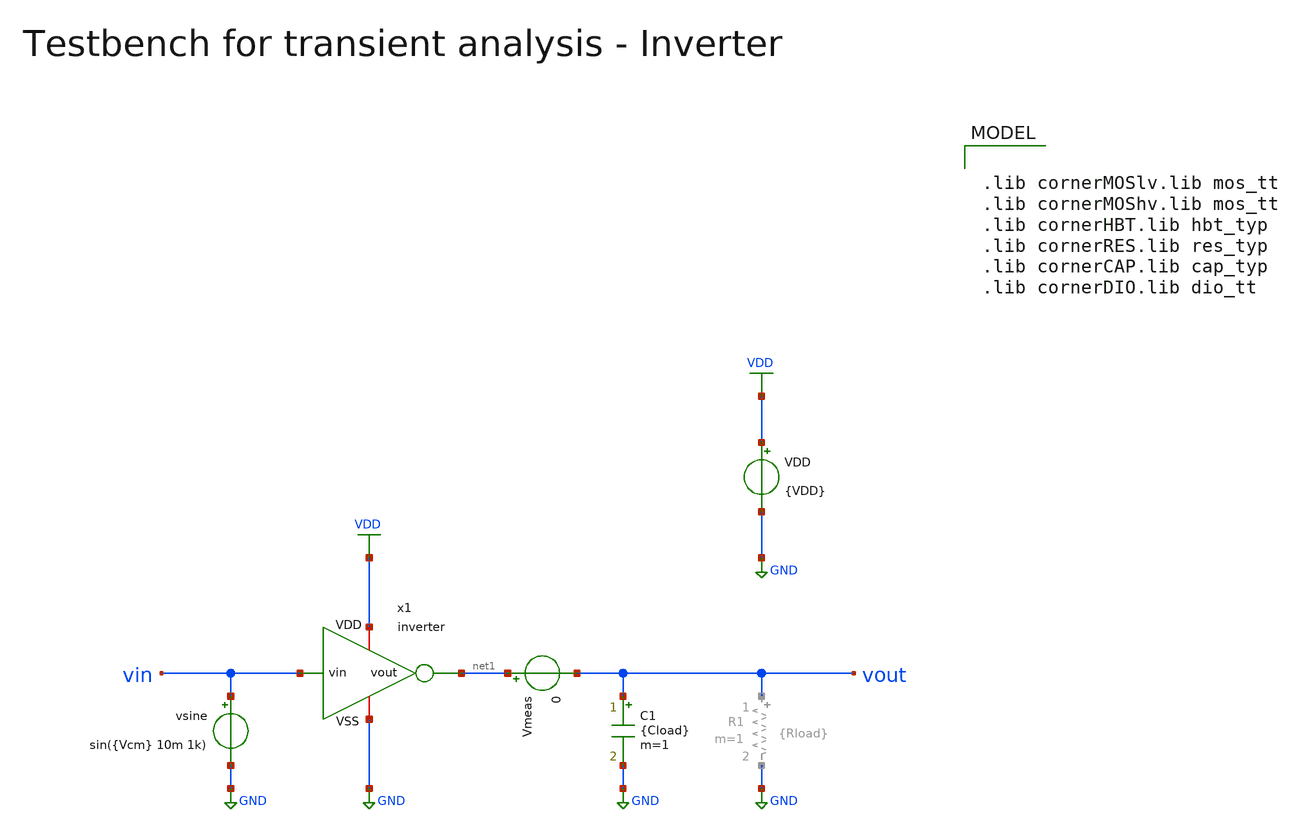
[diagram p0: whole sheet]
** sch_path: macros/inverter/testbenches/inverter_tb_tran.sch
**.subckt inverter_tb_tran
VDD VDD GND {VDD}
vsine vin GND sin({Vcm} 10m 1k)
Vmeas net1 vout 0
C1 vout GND {Cload} m=1
x1 VDD vin net1 GND inverter
**** begin user architecture code


* .include ../../netlist/pex/inverter_top_pex.spice
.param VDD=1.5
.csparam VDD=VDD
.param Vcm=VDD/2
.param temp=27
.param Cload=10p
.param Rload=1k
.options savecurrents klu method=gear reltol=1e-4 abstol=1e-15 gmin=1e-15
.control

* save vin vinp vinn voutp voutn vout
save all

* Operating Point Analysis
op
remzerovec
write @schname\.raw
set appendwrite

* Transient Analysis
* Sine Input
tran 1u 5m
* Pulse Input
* tran 500n 1m
write @schname\.raw

* Plotting
plot vin vout
* plot i(VDD)

* Measurements
meas tran vin_peak MAX v(vin)
meas tran vout_peak MAX v(vout)

let Adm = vout_peak / vin_peak
let Adm_dB = vdb(Adm)
print Adm_dB

meas tran vout_pp_max MAX v(vout)
meas tran vout_pp_min MIN v(vout)
let vout_pp = vout_pp_max - vout_pp_min
print vout_pp

* Calculation of Power Consumption & Efficiency
let tstart = 1m
let tstop = 2m
let PDD_inst = VDD * -i(VDD)
meas tran PDD_int INTEG PDD_inst from=tstart to=tstop
let PDD = 1/(tstop - tstart) * PDD_int * 1e3
echo PDD = $&PDD mW

let Pout_inst = v(vout) * i(Vmeas)
meas tran Pout_int INTEG Pout_inst from=tstart to=tstop
let Pout = 1/(tstop - tstart) * Pout_int * 1e3
echo Pout = $&Pout mW

let efficiency = Pout / PDD * 100
echo efficiency = $&efficiency %

* Write Data
unset appendwrite
set wr_vecnames
set wr_singlescale
wrdata $PROJECT_PATH/scripts/plot_simulations/data/inverter_top_tb_tran.txt v(vin) v(vout)

*quit
.endc



.lib cornerMOSlv.lib mos_tt
.lib cornerMOShv.lib mos_tt
.lib cornerHBT.lib hbt_typ
.lib cornerRES.lib res_typ
.lib cornerCAP.lib cap_typ
.lib cornerDIO.lib dio_tt

**** end user architecture code
**.ends
.GLOBAL GND
.GLOBAL VDD
.end
